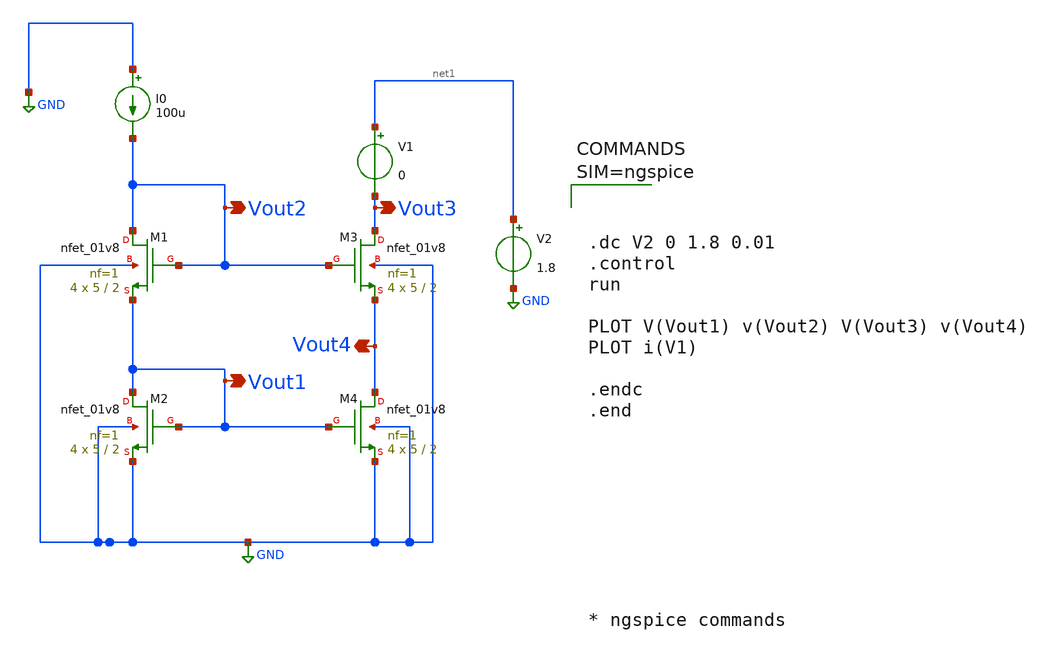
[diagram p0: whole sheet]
** sch_path: spice/cas_cmnmos.sch
**.subckt cas_cmnmos Vout1 Vout2 Vout3 Vout4
*.opin Vout1
*.opin Vout2
*.opin Vout3
*.opin Vout4
XM2 Vout1 Vout1 GND GND sky130_fd_pr__nfet_01v8 L=2 W=5 nf=1 ad='int((1 + 1)/2) * 5 / 1 * 0.29' as='int((1 + 2)/2) * 5 / 1 * 0.29'
+ pd='2*int((1 + 1)/2) * (5 / 1 + 0.29)' ps='2*int((1 + 2)/2) * (5 / 1 + 0.29)' nrd='0.29 / 5 ' nrs='0.29 / 5 '
+ sa=0 sb=0 sd=0 mult=4 m=4
XM1 Vout2 Vout2 Vout1 GND sky130_fd_pr__nfet_01v8 L=2 W=5 nf=1 ad='int((1 + 1)/2) * 5 / 1 * 0.29' as='int((1 + 2)/2) * 5 / 1 * 0.29'
+ pd='2*int((1 + 1)/2) * (5 / 1 + 0.29)' ps='2*int((1 + 2)/2) * (5 / 1 + 0.29)' nrd='0.29 / 5 ' nrs='0.29 / 5 '
+ sa=0 sb=0 sd=0 mult=4 m=4
XM3 Vout3 Vout2 Vout4 GND sky130_fd_pr__nfet_01v8 L=2 W=5 nf=1 ad='int((1 + 1)/2) * 5 / 1 * 0.29' as='int((1 + 2)/2) * 5 / 1 * 0.29'
+ pd='2*int((1 + 1)/2) * (5 / 1 + 0.29)' ps='2*int((1 + 2)/2) * (5 / 1 + 0.29)' nrd='0.29 / 5 ' nrs='0.29 / 5 '
+ sa=0 sb=0 sd=0 mult=4 m=4
XM4 Vout4 Vout1 GND GND sky130_fd_pr__nfet_01v8 L=2 W=5 nf=1 ad='int((1 + 1)/2) * 5 / 1 * 0.29' as='int((1 + 2)/2) * 5 / 1 * 0.29'
+ pd='2*int((1 + 1)/2) * (5 / 1 + 0.29)' ps='2*int((1 + 2)/2) * (5 / 1 + 0.29)' nrd='0.29 / 5 ' nrs='0.29 / 5 '
+ sa=0 sb=0 sd=0 mult=4 m=4
V1 net1 Vout3 0
V2 net1 GND 1.8
I0 GND Vout2 100u
**** begin user architecture code

** opencircuitdesign pdks install
.lib $::SKYWATER_MODELS/sky130.lib.spice tt





.dc V2 0 1.8 0.01
.control
run

PLOT V(Vout1) v(Vout2) V(Vout3) v(Vout4)
PLOT i(V1)

.endc
.end









* ngspice commands



**** end user architecture code
**.ends
.GLOBAL GND
.end
